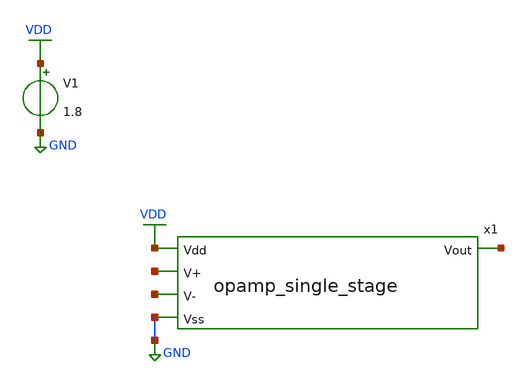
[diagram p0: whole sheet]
** sch_path: analog/schematics/opamp_single_stage_tb.sch
**.subckt opamp_single_stage_tb
x1 VDD net1 net2 net3 GND opamp_single_stage
V1 VDD GND 1.8
**.ends

* expanding   symbol:  opamp_single_stage.sym # of pins=5
** sym_path: analog/schematics/opamp_single_stage.sym
** sch_path: analog/schematics/opamp_single_stage.sch
.subckt opamp_single_stage Vdd Vout V+ V- Vss
*.opin Vout
*.ipin Vdd
*.ipin Vss
*.ipin V+
*.ipin V-
XM3 net1 V+ net2 Vss sky130_fd_pr__nfet_01v8 L=0.25 W=1 nf=1 ad='int((nf+1)/2) * W/nf * 0.29' as='int((nf+2)/2) * W/nf * 0.29'
+ pd='2*int((nf+1)/2) * (W/nf + 0.29)' ps='2*int((nf+2)/2) * (W/nf + 0.29)' nrd='0.29 / W' nrs='0.29 / W'
+ sa=0 sb=0 sd=0 mult=1 m=1
XM4 Vout V- net2 Vss sky130_fd_pr__nfet_01v8 L=0.25 W=1 nf=1 ad='int((nf+1)/2) * W/nf * 0.29' as='int((nf+2)/2) * W/nf * 0.29'
+ pd='2*int((nf+1)/2) * (W/nf + 0.29)' ps='2*int((nf+2)/2) * (W/nf + 0.29)' nrd='0.29 / W' nrs='0.29 / W'
+ sa=0 sb=0 sd=0 mult=1 m=1
XM5 net2 net3 Vss Vss sky130_fd_pr__nfet_01v8 L=0.25 W=1 nf=1 ad='int((nf+1)/2) * W/nf * 0.29' as='int((nf+2)/2) * W/nf * 0.29'
+ pd='2*int((nf+1)/2) * (W/nf + 0.29)' ps='2*int((nf+2)/2) * (W/nf + 0.29)' nrd='0.29 / W' nrs='0.29 / W'
+ sa=0 sb=0 sd=0 mult=1 m=1
XM1 net1 net1 Vdd Vdd sky130_fd_pr__pfet_01v8 L=0.25 W=1 nf=1 ad='int((nf+1)/2) * W/nf * 0.29' as='int((nf+2)/2) * W/nf * 0.29'
+ pd='2*int((nf+1)/2) * (W/nf + 0.29)' ps='2*int((nf+2)/2) * (W/nf + 0.29)' nrd='0.29 / W' nrs='0.29 / W'
+ sa=0 sb=0 sd=0 mult=1 m=1
XM2 Vout net1 Vdd Vdd sky130_fd_pr__pfet_01v8 L=0.25 W=1 nf=1 ad='int((nf+1)/2) * W/nf * 0.29' as='int((nf+2)/2) * W/nf * 0.29'
+ pd='2*int((nf+1)/2) * (W/nf + 0.29)' ps='2*int((nf+2)/2) * (W/nf + 0.29)' nrd='0.29 / W' nrs='0.29 / W'
+ sa=0 sb=0 sd=0 mult=1 m=1
XM6 net3 net3 Vss Vss sky130_fd_pr__nfet_01v8 L=0.25 W=1 nf=1 ad='int((nf+1)/2) * W/nf * 0.29' as='int((nf+2)/2) * W/nf * 0.29'
+ pd='2*int((nf+1)/2) * (W/nf + 0.29)' ps='2*int((nf+2)/2) * (W/nf + 0.29)' nrd='0.29 / W' nrs='0.29 / W'
+ sa=0 sb=0 sd=0 mult=1 m=1
XR1 net3 Vdd net4 sky130_fd_pr__res_high_po W=2.5 L=0.1 mult=1 m=1
.ends

.GLOBAL GND
.GLOBAL VDD
.end
